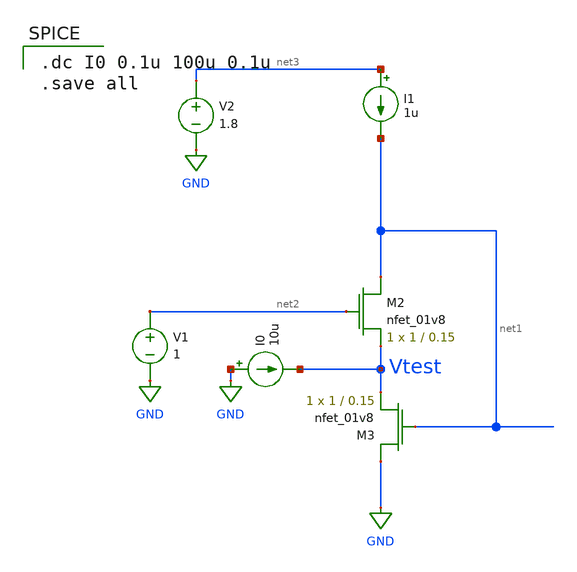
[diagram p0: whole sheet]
** sch_path: FVF_test.sch
**.subckt FVF_test
XM2 net1 net2 Vtest GND sky130_fd_pr__nfet_01v8 L=0.15 W=1 nf=1 ad='int((nf+1)/2) * W/nf * 0.29' as='int((nf+2)/2) * W/nf * 0.29'
+ pd='2*int((nf+1)/2) * (W/nf + 0.29)' ps='2*int((nf+2)/2) * (W/nf + 0.29)' nrd='0.29 / W' nrs='0.29 / W'
+ sa=0 sb=0 sd=0 mult=1 m=1
XM3 GND net1 Vtest GND sky130_fd_pr__nfet_01v8 L=0.15 W=1 nf=1 ad='int((nf+1)/2) * W/nf * 0.29' as='int((nf+2)/2) * W/nf * 0.29'
+ pd='2*int((nf+1)/2) * (W/nf + 0.29)' ps='2*int((nf+2)/2) * (W/nf + 0.29)' nrd='0.29 / W' nrs='0.29 / W'
+ sa=0 sb=0 sd=0 mult=1 m=1
V1 net2 GND 1
V2 net3 GND 1.8
I0 GND Vtest 10u
I1 net3 net1 1u
**** begin user architecture code

.dc I0 0.1u 100u 0.1u
.save all


.lib $::SKYWATER_MODELS/sky130.lib.spice tt

**** end user architecture code
**.ends
.GLOBAL GND
.end
